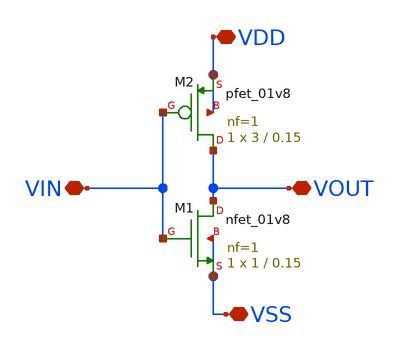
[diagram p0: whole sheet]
** sch_path: xschem/DC_DC_Converter_xschem/OTHERS/DC_DC_Converter_JV11/Delay_block_revised/inverter_delay.sch
**.subckt inverter_delay VDD VOUT VSS VIN
*.iopin VDD
*.iopin VOUT
*.iopin VSS
*.iopin VIN
XM1 VOUT VIN VSS VSS sky130_fd_pr__nfet_01v8 L=0.15 W=1 nf=1 ad='int((nf+1)/2) * W/nf * 0.29' as='int((nf+2)/2) * W/nf * 0.29'
+ pd='2*int((nf+1)/2) * (W/nf + 0.29)' ps='2*int((nf+2)/2) * (W/nf + 0.29)' nrd='0.29 / W' nrs='0.29 / W'
+ sa=0 sb=0 sd=0 mult=1 m=1
XM2 VOUT VIN VDD VDD sky130_fd_pr__pfet_01v8 L=0.15 W=3 nf=1 ad='int((nf+1)/2) * W/nf * 0.29' as='int((nf+2)/2) * W/nf * 0.29'
+ pd='2*int((nf+1)/2) * (W/nf + 0.29)' ps='2*int((nf+2)/2) * (W/nf + 0.29)' nrd='0.29 / W' nrs='0.29 / W'
+ sa=0 sb=0 sd=0 mult=1 m=1
**.ends
.end
